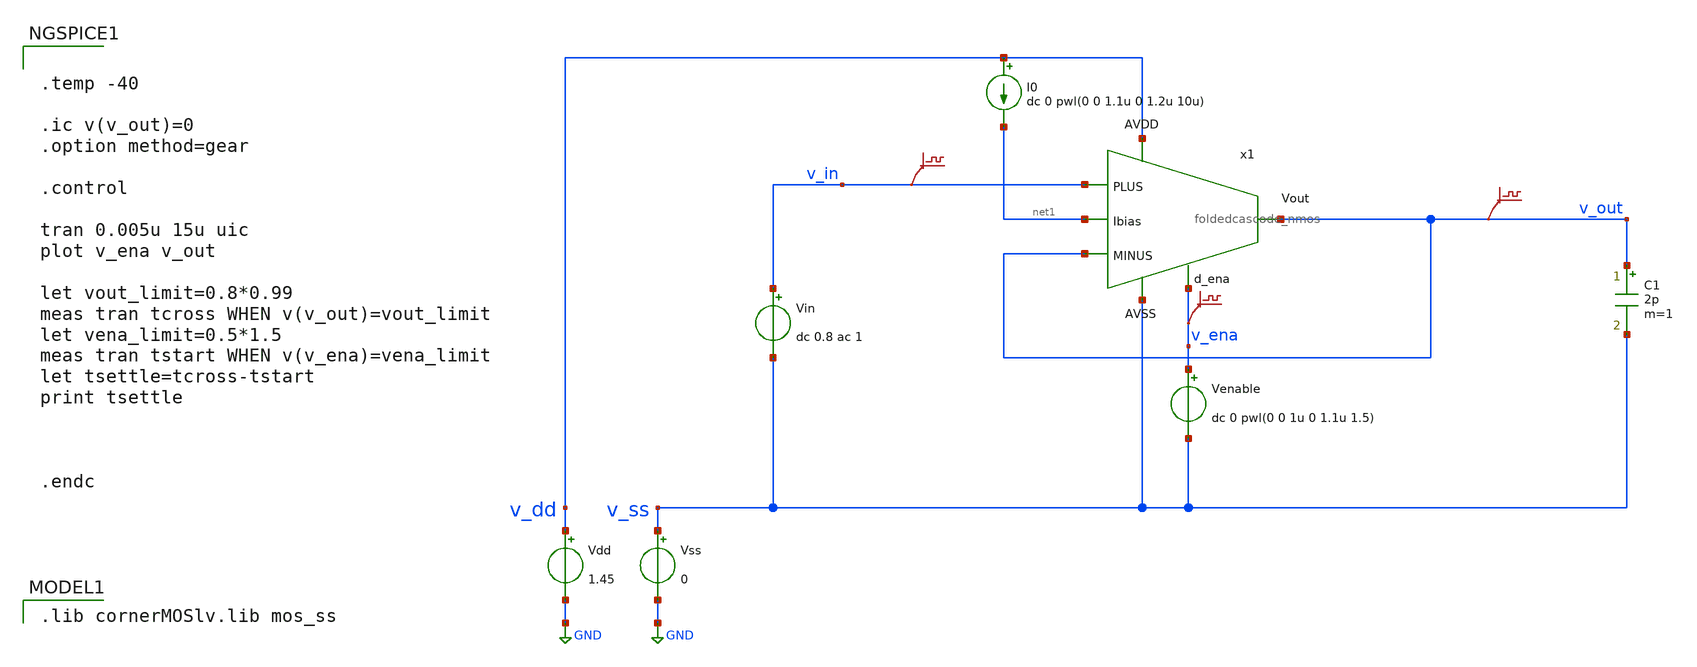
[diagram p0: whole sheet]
** sch_path: Designs/otas/tb_foldedcascode_nmos_tran.sch
* (c) 2025 Thesis_HP, Apache-2.0 license
**.subckt tb_foldedcascode_nmos_tran
Vdd v_dd GND 1.45
Vss v_ss GND 0
C1 v_out v_ss 2p m=1
Vin v_in v_ss dc 0.8 ac 1
.save v(v_in)
.save v(v_out)
x1 v_dd v_in v_out v_out net1 v_ena v_ss foldedcascode_nmos
Venable v_ena v_ss dc 0 pwl(0 0 1u 0 1.1u 1.5)
.save v(v_ena)
I0 v_dd net1 dc 0 pwl(0 0 1.1u 0 1.2u 10u)
**** begin user architecture code
 .lib cornerMOSlv.lib mos_ss



.temp -40

.ic v(v_out)=0
.option method=gear

.control

tran 0.005u 15u uic
plot v_ena v_out

let vout_limit=0.8*0.99
meas tran tcross WHEN v(v_out)=vout_limit
let vena_limit=0.5*1.5
meas tran tstart WHEN v(v_ena)=vena_limit
let tsettle=tcross-tstart
print tsettle



.endc


**** end user architecture code
**.ends

* expanding   symbol:  foldedcascode_nmos.sym # of pins=7
** sym_path: Designs/otas/foldedcascode_nmos.sym
** sch_path: Designs/otas/foldedcascode_nmos.sch
.subckt foldedcascode_nmos AVDD PLUS MINUS Vout Ibias d_ena AVSS
*.ipin PLUS
*.ipin MINUS
*.opin Vout
*.ipin AVDD
*.ipin AVSS
*.ipin Ibias
*.ipin d_ena
XM1 net5 PLUS net1 AVSS sg13_lv_nmos w=5u l=1u ng=1 m=1 mm_ok=1
XMt net11 Ibias AVSS AVSS sg13_lv_nmos w=5.5u l=5u ng=3 m=1 mm_ok=1
XM4 net3 net4 AVSS AVSS sg13_lv_nmos w=1u l=0.5u ng=1 m=1 mm_ok=1
XM3 net2 net4 AVSS AVSS sg13_lv_nmos w=1u l=0.5u ng=1 m=1 mm_ok=1
XM2 net6 MINUS net1 AVSS sg13_lv_nmos w=5u l=1u ng=1 m=1 mm_ok=1
XM7 net4 net9 net2 AVSS sg13_lv_nmos w=1.5u l=0.5u ng=1 m=1 mm_ok=1
XM8 Vout net9 net3 AVSS sg13_lv_nmos w=1.5u l=0.5u ng=1 m=1 mm_ok=1
XM5 net4 net8 net5 AVDD sg13_lv_pmos w=6u l=0.5u ng=1 m=1 mm_ok=1
XM9 net5 net7 AVDD AVDD sg13_lv_pmos w=6u l=0.5u ng=1 m=1 mm_ok=1
XM6 Vout net8 net6 AVDD sg13_lv_pmos w=6u l=0.5u ng=1 m=1 mm_ok=1
XM0 net6 net7 AVDD AVDD sg13_lv_pmos w=6u l=0.5u ng=1 m=1 mm_ok=1
XMb Ibias Ibias AVSS AVSS sg13_lv_nmos w=4u l=5u ng=2 m=1 mm_ok=1
XM11 net8 net8 net7 AVDD sg13_lv_pmos w=6u l=0.5u ng=2 m=1 mm_ok=1
XM12 net7 net7 AVDD AVDD sg13_lv_pmos w=6u l=0.5u ng=2 m=1 mm_ok=1
XM13 net12 net7 AVDD AVDD sg13_lv_pmos w=6u l=0.5u ng=2 m=1 mm_ok=1
XM14 net9 net9 AVSS AVSS sg13_lv_nmos w=1.5u l=0.5u ng=1 m=1 mm_ok=1
XMb1 net10 Ibias AVSS AVSS sg13_lv_nmos w=4u l=5u ng=2 m=1 mm_ok=1
Vmeas net8 net10 0
.save i(vmeas)
Vmeas1 net1 net11 0
.save i(vmeas1)
Vmeas2 net12 net9 0
.save i(vmeas2)
XMdecoup1 AVSS Ibias AVSS AVSS sg13_lv_nmos w=8u l=1u ng=4 m=1 mm_ok=1
XMdecoup2 AVSS net9 AVSS AVSS sg13_lv_nmos w=8u l=1u ng=4 m=1 mm_ok=1
XMdecoup3 AVDD net7 AVDD AVDD sg13_lv_pmos w=12u l=0.5u ng=4 m=1 mm_ok=1
XMdecoup4 AVDD net8 AVDD AVDD sg13_lv_pmos w=12u l=0.5u ng=4 m=1 mm_ok=1
XMpd3 ena ena_n AVSS AVSS sg13_lv_nmos w=1u l=0.13u ng=1 m=1 mm_ok=1
XMpd4 ena ena_n AVDD AVDD sg13_lv_pmos w=1u l=0.13u ng=1 m=1 mm_ok=1
XMpd1 ena_n d_ena AVSS AVSS sg13_lv_nmos w=1u l=0.13u ng=1 m=1 mm_ok=1
XMpd2 ena_n d_ena AVDD AVDD sg13_lv_pmos w=1u l=0.13u ng=1 m=1 mm_ok=1
XMpd5 Ibias ena_n AVSS AVSS sg13_lv_nmos w=1u l=0.13u ng=1 m=1 mm_ok=1
XMpd6 Ibias ena Ibias AVSS sg13_lv_nmos w=1u l=0.13u ng=1 m=1 mm_ok=1
XMpd7 net7 ena AVDD AVDD sg13_lv_pmos w=1u l=0.13u ng=1 m=1 mm_ok=1
XMpd8 net8 ena AVDD AVDD sg13_lv_pmos w=1u l=0.13u ng=1 m=1 mm_ok=1
XMpd9 net4 ena_n AVSS AVSS sg13_lv_nmos w=1u l=0.13u ng=1 m=1 mm_ok=1
XMpd10 net9 ena_n AVSS AVSS sg13_lv_nmos w=1u l=0.13u ng=1 m=1 mm_ok=1
XMpd11 Vout ena_n AVSS AVSS sg13_lv_nmos w=1u l=0.13u ng=1 m=1 mm_ok=1
.ends

.GLOBAL GND
.end
